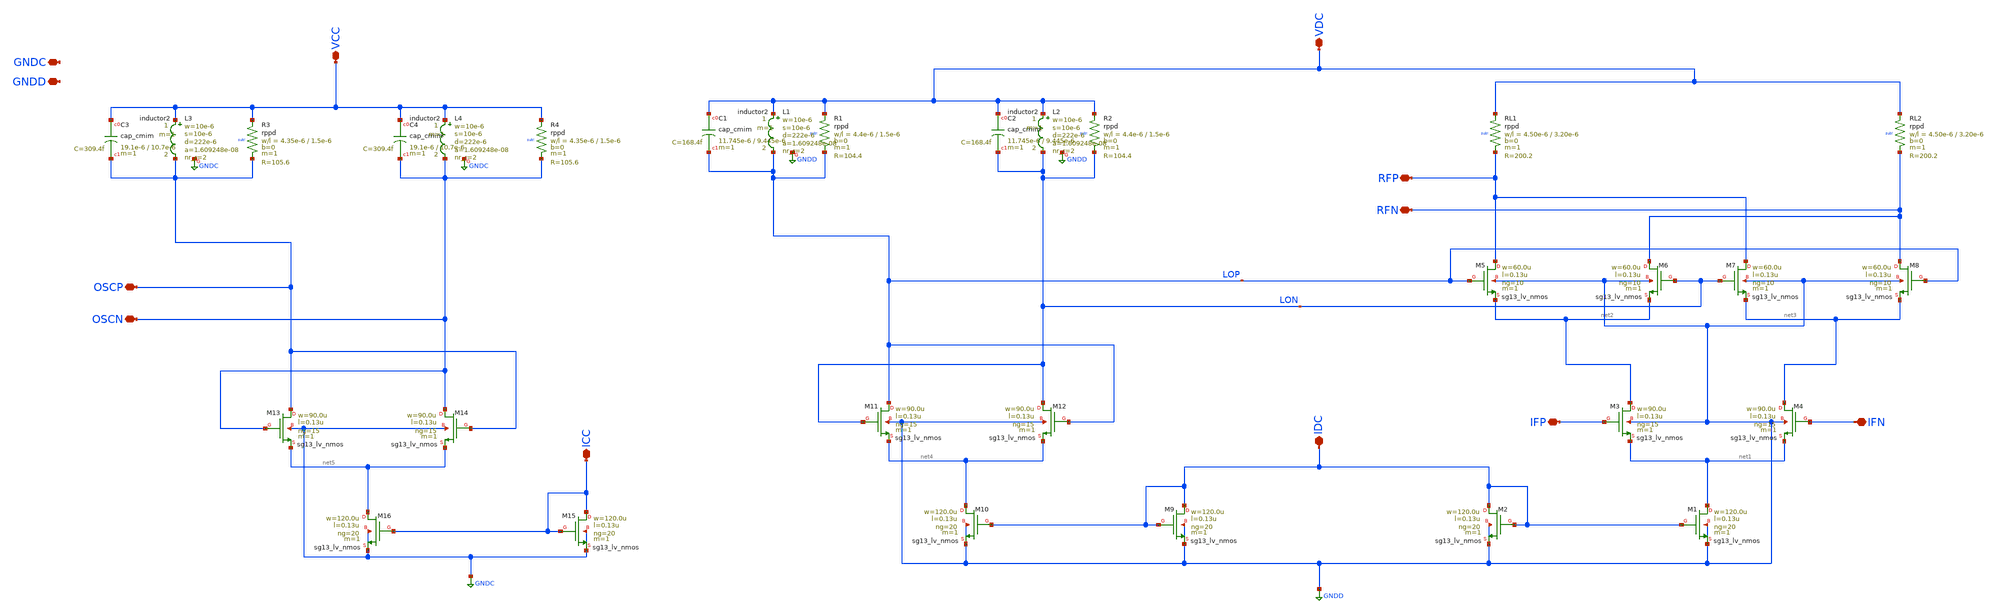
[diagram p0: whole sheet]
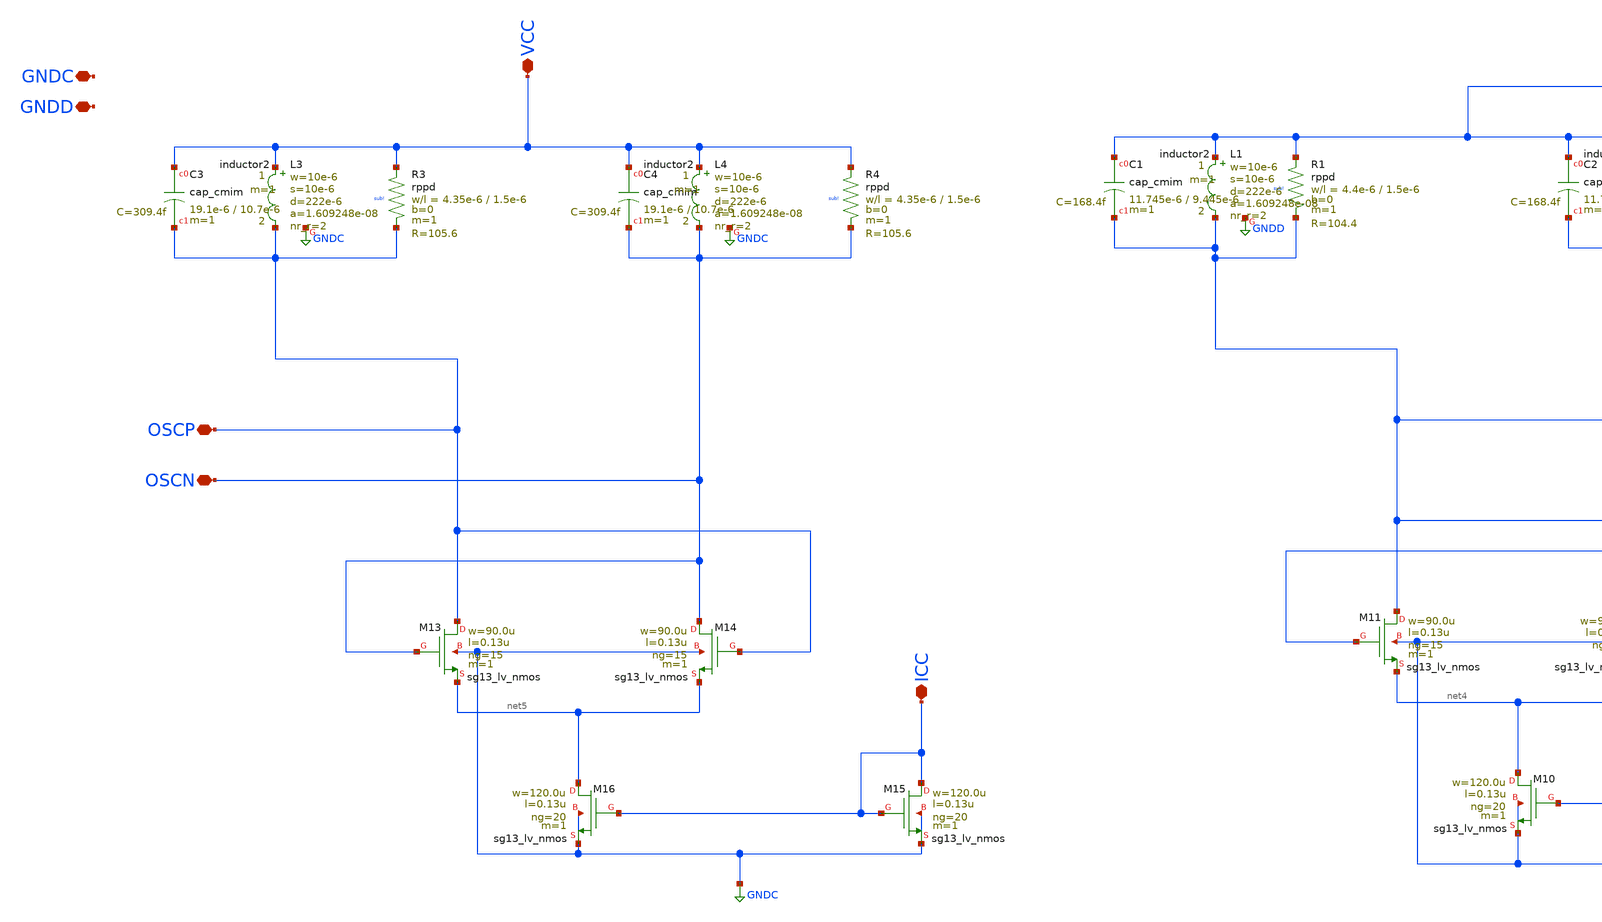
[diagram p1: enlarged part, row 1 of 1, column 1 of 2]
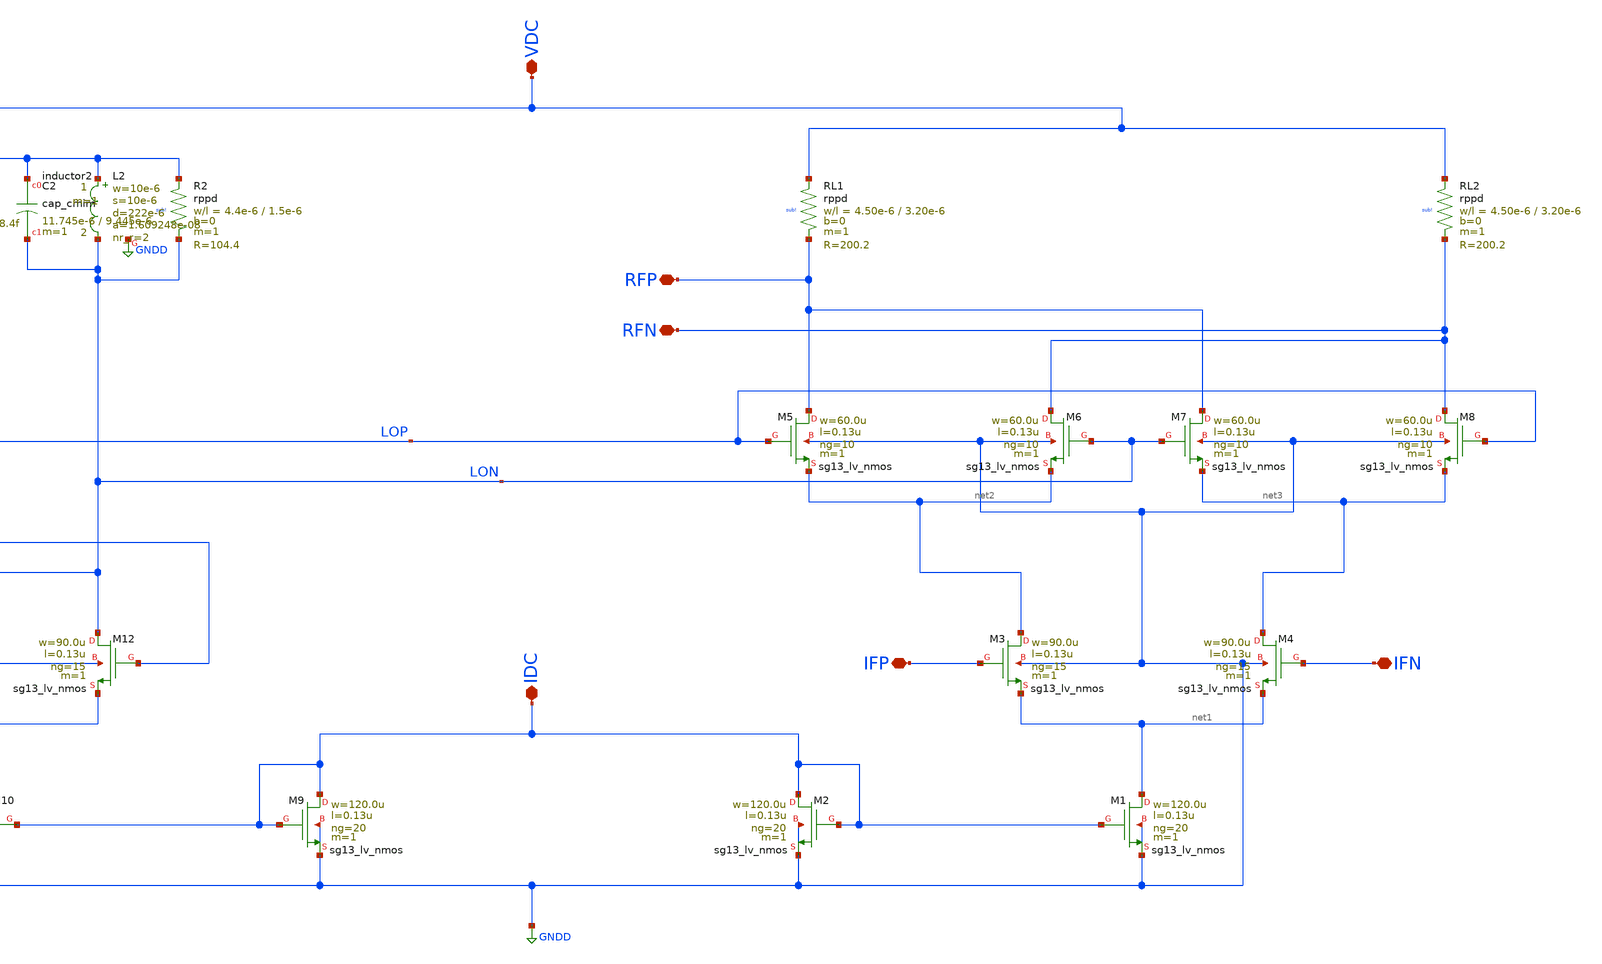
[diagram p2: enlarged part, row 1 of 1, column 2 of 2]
** sch_path: TO_Apr2025/Mixer5GHz/xschem/Mixer5GHz.sch
**.subckt Mixer5GHz RFN RFP VDC IFP IFN IDC OSCN OSCP VCC ICC GNDC GNDD
*.iopin RFN
*.iopin RFP
*.iopin VDC
*.iopin IFP
*.iopin IFN
*.iopin IDC
*.iopin OSCN
*.iopin OSCP
*.iopin VCC
*.iopin ICC
*.iopin GNDC
*.iopin GNDD
XM6 RFN LON net2 GNDD sg13_lv_nmos w=60.0u l=0.13u ng=10 m=1 mm_ok=1
XRL2 VDC RFN sub! rppd w=4.50e-6 l=3.20e-6 m=1 b=0 mm_ok=1
XRL1 VDC RFP sub! rppd w=4.50e-6 l=3.20e-6 m=1 b=0 mm_ok=1
XM8 RFN LOP net3 GNDD sg13_lv_nmos w=60.0u l=0.13u ng=10 m=1 mm_ok=1
XM7 RFP LON net3 GNDD sg13_lv_nmos w=60.0u l=0.13u ng=10 m=1 mm_ok=1
XM5 RFP LOP net2 GNDD sg13_lv_nmos w=60.0u l=0.13u ng=10 m=1 mm_ok=1
XM4 net3 IFN net1 GNDD sg13_lv_nmos w=90.0u l=0.13u ng=15 m=1 mm_ok=1
XM3 net2 IFP net1 GNDD sg13_lv_nmos w=90.0u l=0.13u ng=15 m=1 mm_ok=1
XM2 IDC IDC GNDD GNDD sg13_lv_nmos w=120.0u l=0.13u ng=20 m=1 mm_ok=1
XM1 net1 IDC GNDD GNDD sg13_lv_nmos w=120.0u l=0.13u ng=20 m=1 mm_ok=1
XM11 LOP LON net4 GNDD sg13_lv_nmos w=90.0u l=0.13u ng=15 m=1 mm_ok=1
XM12 LON LOP net4 GNDD sg13_lv_nmos w=90.0u l=0.13u ng=15 m=1 mm_ok=1
XM9 IDC IDC GNDD GNDD sg13_lv_nmos w=120.0u l=0.13u ng=20 m=1 mm_ok=1
XM10 net4 IDC GNDD GNDD sg13_lv_nmos w=120.0u l=0.13u ng=20 m=1 mm_ok=1
XC1 VDC LOP cap_cmim w=11.745e-6 l=9.445e-6 m=1 mm_ok=1
XR1 VDC LOP sub! rppd w=4.4e-6 l=1.5e-6 m=1 b=0 mm_ok=1
XC2 VDC LON cap_cmim w=11.745e-6 l=9.445e-6 m=1 mm_ok=1
XR2 VDC LON sub! rppd w=4.4e-6 l=1.5e-6 m=1 b=0 mm_ok=1
XM13 OSCP OSCN net5 GNDC sg13_lv_nmos w=90.0u l=0.13u ng=15 m=1 mm_ok=1
XM14 OSCN OSCP net5 GNDC sg13_lv_nmos w=90.0u l=0.13u ng=15 m=1 mm_ok=1
XM15 ICC ICC GNDC GNDC sg13_lv_nmos w=120.0u l=0.13u ng=20 m=1 mm_ok=1
XM16 net5 ICC GNDC GNDC sg13_lv_nmos w=120.0u l=0.13u ng=20 m=1 mm_ok=1
XC3 VCC OSCP cap_cmim w=19.1e-6 l=10.7e-6 m=1 mm_ok=1
XR3 VCC OSCP sub! rppd w=4.35e-6 l=1.5e-6 m=1 b=0 mm_ok=1
XC4 VCC OSCN cap_cmim w=19.1e-6 l=10.7e-6 m=1 mm_ok=1
XR4 VCC OSCN sub! rppd w=4.35e-6 l=1.5e-6 m=1 b=0 mm_ok=1
XL1 VDC LOP GNDD inductor2 w=10e-6 s=10e-6 d=222e-6 nr_r=2 m=1
XL2 VDC LON GNDD inductor2 w=10e-6 s=10e-6 d=222e-6 nr_r=2 m=1
XL3 VCC OSCP GNDC inductor2 w=10e-6 s=10e-6 d=222e-6 nr_r=2 m=1
XL4 VCC OSCN GNDC inductor2 w=10e-6 s=10e-6 d=222e-6 nr_r=2 m=1
**.ends
.end
